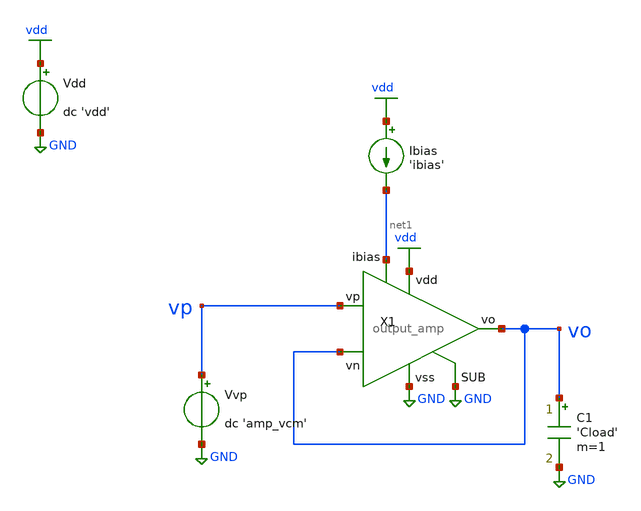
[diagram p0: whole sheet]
** sch_path: tb/output_amp/tb_amp_power.sch
**.subckt tb_amp_power
X1 vdd vo vp vo net1 GND GND output_amp
Vdd vdd GND dc 'vdd'
Vvp vp GND dc 'amp_vcm'
Ibias vdd net1 'ibias'
C1 vo GND 'Cload' m=1
**** begin user architecture code


.lib 'models_dir'/cornerMOShv.lib 'mos_corner'
.lib 'models_dir'/cornerCAP.lib cap_typ
.option TEMP='temperature'
.option warn=1
.control
save all
op
set wr_singlescale
wrdata 'simpath'/'filename'_'N'.data -I(Vdd)
quit
.endc


**** end user architecture code
**.ends
.GLOBAL GND
.GLOBAL vdd
.end
